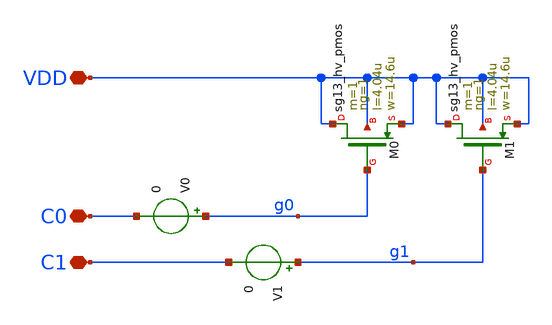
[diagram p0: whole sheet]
** sch_path: xschem/dacbuffer_1chan.sch
**.subckt dacbuffer_1chan VDD C0 C1
*.iopin VDD
*.iopin C0
*.iopin C1
XM1 VDD g1 VDD VDD sg13_hv_pmos w=14.6u l=4.04u ng=1 m=1 mm_ok=1
XM0 VDD g0 VDD VDD sg13_hv_pmos w=14.6u l=4.04u ng=1 m=1 mm_ok=1
V0 g0 C0 0
.save i(v0)
V1 g1 C1 0
.save i(v1)
**.ends
.end
